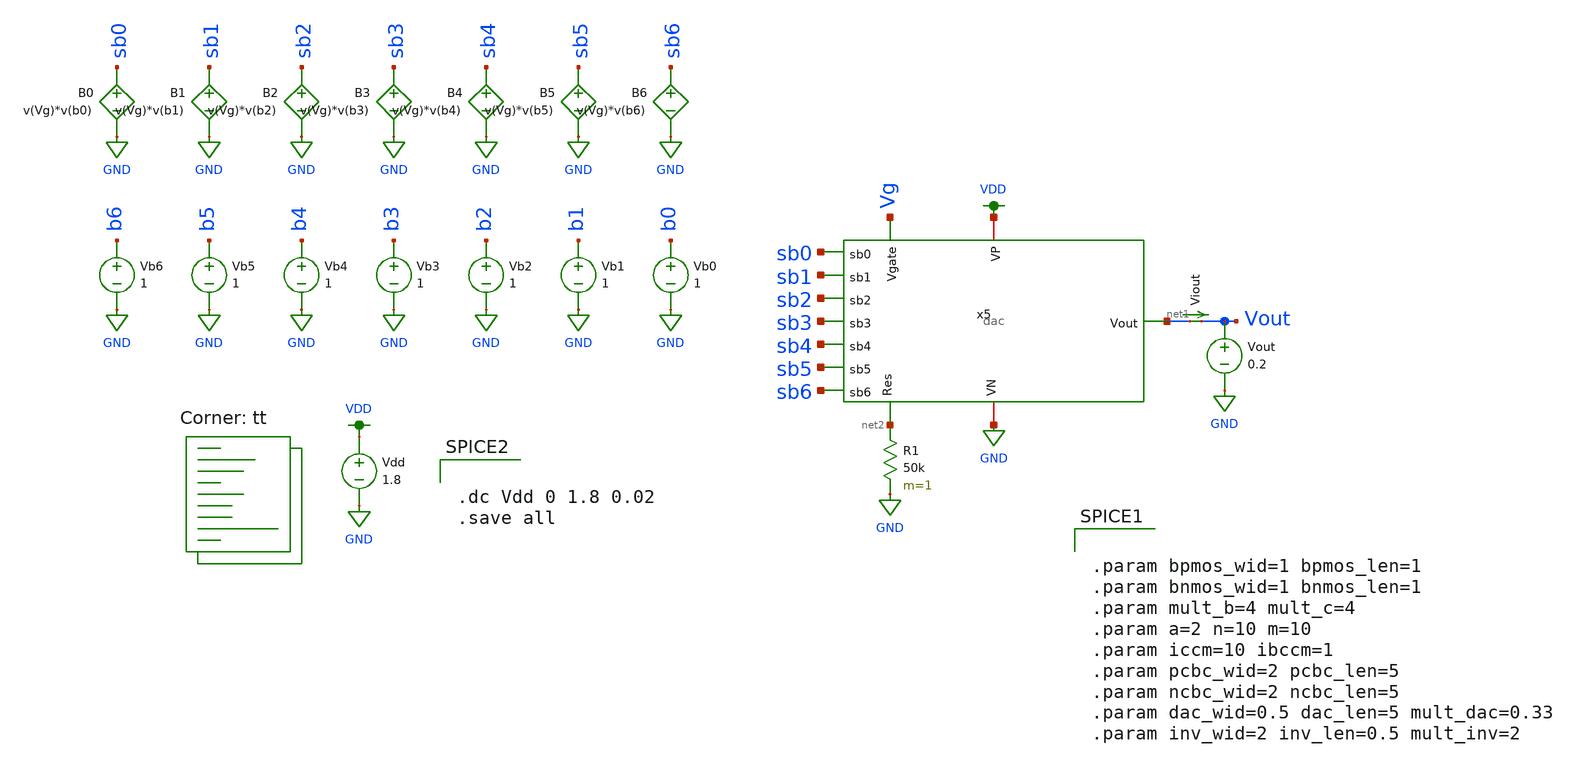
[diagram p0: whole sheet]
** sch_path: Supply Independence and Output Sweeps/test_dac_vdd.sch
**.subckt test_dac_vdd
Vdd VDD GND 1.8
R1 net2 GND 50k m=1
Vout Vout GND 0.2
Viout net1 Vout 0
.save i(viout)
Vb0 b0 GND 1
B0 sb0 GND V=v(Vg)*v(b0)
Vb1 b1 GND 1
B1 sb1 GND V=v(Vg)*v(b1)
Vb2 b2 GND 1
B2 sb2 GND V=v(Vg)*v(b2)
Vb3 b3 GND 1
B3 sb3 GND V=v(Vg)*v(b3)
Vb4 b4 GND 1
B4 sb4 GND V=v(Vg)*v(b4)
Vb5 b5 GND 1
B5 sb5 GND V=v(Vg)*v(b5)
Vb6 b6 GND 1
B6 sb6 GND V=v(Vg)*v(b6)
x5 VDD sb0 sb1 GND sb2 net1 Vg sb3 sb4 sb5 sb6 net2 dac
**** begin user architecture code
.lib $::SKYWATER_MODELS/sky130.lib.spice tt


.dc Vdd 0 1.8 0.02
.save all




.param bpmos_wid=1 bpmos_len=1
.param bnmos_wid=1 bnmos_len=1
.param mult_b=4 mult_c=4
.param a=2 n=10 m=10
.param iccm=10 ibccm=1
.param pcbc_wid=2 pcbc_len=5
.param ncbc_wid=2 ncbc_len=5
.param dac_wid=0.5 dac_len=5 mult_dac=0.33
.param inv_wid=2 inv_len=0.5 mult_inv=2


**** end user architecture code
**.ends
.GLOBAL GND
.GLOBAL VDD
.end
